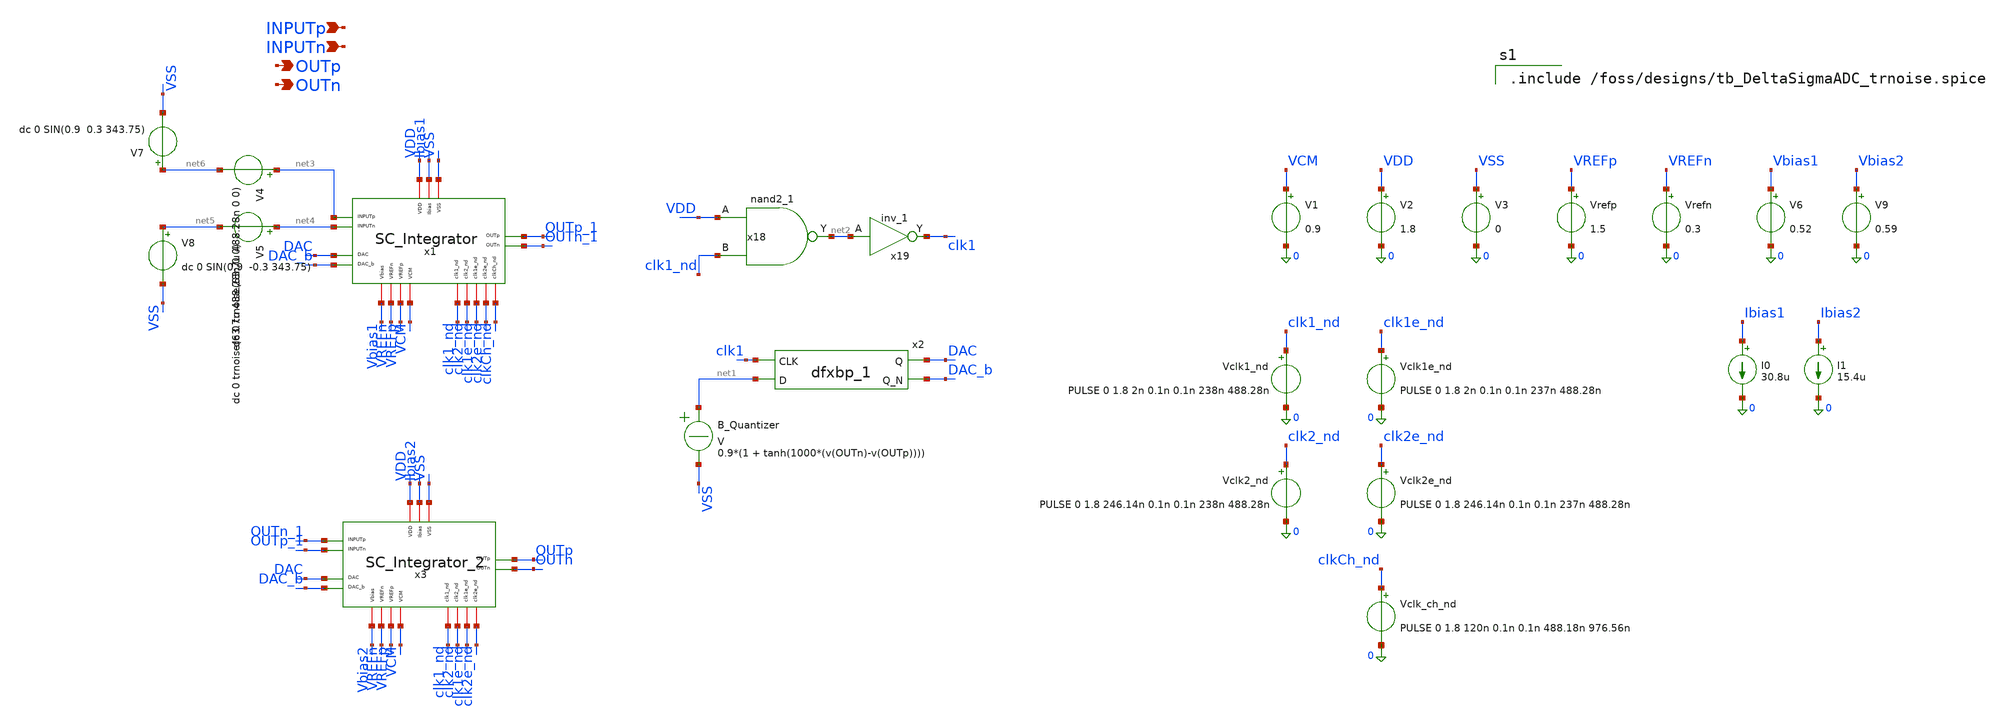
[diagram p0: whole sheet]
** sch_path: xschem/top/DeltaSigmaADC_L2.sch
**.subckt DeltaSigmaADC_L2 OUTp OUTn INPUTp INPUTn
*.opin OUTp
*.opin OUTn
*.ipin INPUTp
*.ipin INPUTn
x1 VDD clk1_nd OUTp_1 net3 VSS clk2_nd net4 OUTn_1 Ibias1 DAC clk1e_nd VCM DAC_b clk2e_nd VREFp
+ VREFn Vbias1 clkCh_nd SC_Integrator
V1 VCM 0 0.9
V2 VDD 0 1.8
I0 Ibias1 0 30.8u
V3 VSS 0 0
Vrefp VREFp 0 1.5
Vrefn VREFn 0 0.3
V6 Vbias1 0 0.52
Vclk1_nd clk1_nd 0 PULSE 0 1.8 2n 0.1n 0.1n 238n 488.28n
Vclk1e_nd clk1e_nd 0 PULSE 0 1.8 2n 0.1n 0.1n 237n 488.28n
Vclk2_nd clk2_nd 0 PULSE 0 1.8 246.14n 0.1n 0.1n 238n 488.28n
Vclk2e_nd clk2e_nd 0 PULSE 0 1.8 246.14n 0.1n 0.1n 237n 488.28n
B_Quantizer net1 VSS V = 0.9*(1 + tanh(1000*(v(OUTn)-v(OUTp))))
x2 clk1 net1 VSS VSS VDD VDD DAC DAC_b sky130_fd_sc_hd__dfxbp_1
x18 VDD clk1_nd VSS VSS VDD VDD net2 sky130_fd_sc_hd__nand2_1
x19 net2 VSS VSS VDD VDD clk1 sky130_fd_sc_hd__inv_1
x3 VDD clk1_nd OUTp OUTn_1 VSS clk2_nd OUTp_1 OUTn Ibias2 DAC clk1e_nd VCM DAC_b clk2e_nd VREFp
+ VREFn Vbias2 SC_Integrator_2
I1 Ibias2 0 15.4u
Vclk_ch_nd clkCh_nd 0 PULSE 0 1.8 120n 0.1n 0.1n 488.18n 976.56n
V4 net3 net6 dc 0 trnoise(63.7u 488.28n 0 0)
V5 net4 net5 dc 0 trnoise(63.7u 488.28n 0 0)
V7 net6 VSS dc 0 SIN(0.9 0.3 343.75)
V8 net5 VSS dc 0 SIN(0.9 -0.3 343.75)
V9 Vbias2 0 0.59
**** begin user architecture code

.include /foss/designs/tb_DeltaSigmaADC_trnoise.spice

**** end user architecture code
**.ends

* expanding   symbol:  Analog/SC_Integrator.sym # of pins=18
** sym_path: xschem/lib/Analog/SC_Integrator.sym
** sch_path: xschem/lib/Analog/SC_Integrator.sch
.subckt SC_Integrator VDD clk1_nd OUTp INPUTp VSS clk2_nd INPUTn OUTn Ibias DAC clk1e_nd VCM DAC_b
+ clk2e_nd VREFp VREFn Vbias clkCh_nd
*.iopin clk2e_nd
*.iopin clk1e_nd
*.iopin clk2_nd
*.iopin clk1_nd
*.iopin VDD
*.iopin VSS
*.iopin VCM
*.iopin Ibias
*.ipin INPUTp
*.ipin INPUTn
*.iopin VREFp
*.iopin VREFn
*.iopin Vbias
*.ipin DAC
*.ipin DAC_b
*.opin OUTp
*.opin OUTn
*.iopin clkCh_nd
x1 VDD Ibias net13 OTA_OUTp OTA_OUTn net4 VSS CMFB FullyDiffOTA
x14 DAC_b clk2_nd VSS VSS VDD VDD clkDn_b sky130_fd_sc_hd__nand2_1
x15 clkDn_b VSS VSS VDD VDD clkDn sky130_fd_sc_hd__inv_1
x16 DAC clk2_nd VSS VSS VDD VDD clkDp_b sky130_fd_sc_hd__nand2_1
x17 clkDp_b VSS VSS VDD VDD clkDp sky130_fd_sc_hd__inv_1
x18 VDD clk1_nd VSS VSS VDD VDD clk1_b sky130_fd_sc_hd__nand2_1
x19 clk1_b VSS VSS VDD VDD clk1 sky130_fd_sc_hd__inv_1
x20 VDD clk2_nd VSS VSS VDD VDD clk2_b sky130_fd_sc_hd__nand2_1
x21 clk2_b VSS VSS VDD VDD clk2 sky130_fd_sc_hd__inv_1
x10 VDD clk1e_nd VSS VSS VDD VDD clk1e_b sky130_fd_sc_hd__nand2_1
x25 clk1e_b VSS VSS VDD VDD clk1e sky130_fd_sc_hd__inv_1
x26 VDD clk2e_nd VSS VSS VDD VDD clk2e_b sky130_fd_sc_hd__nand2_1
x27 clk2e_b VSS VSS VDD VDD clk2e sky130_fd_sc_hd__inv_1
XC16 net1 net2 sky130_fd_pr__cap_mim_m3_2 W=15 L=10 MF=6 m=6
XC17 net1 net2 sky130_fd_pr__cap_mim_m3_1 W=19 L=10 MF=6 m=6
XC2 OUTp INn sky130_fd_pr__cap_mim_m3_2 W=15 L=10 MF=20 m=20
XC3 OUTp INn sky130_fd_pr__cap_mim_m3_1 W=19 L=10 MF=20 m=20
XM2 VREFp clkDp_b net7 VDD sky130_fd_pr__pfet_01v8 L=0.15 W=2 nf=1 ad='int((1 + 1)/2) * 2 / 1 * 0.29'
+ as='int((1 + 2)/2) * 2 / 1 * 0.29' pd='2*int((1 + 1)/2) * (2 / 1 + 0.29)' ps='2*int((1 + 2)/2) * (2 / 1 + 0.29)'
+ nrd='0.29 / 2 ' nrs='0.29 / 2 ' sa=0 sb=0 sd=0 mult=1 m=1
XM1 VREFp clkDn_b net3 VDD sky130_fd_pr__pfet_01v8 L=0.15 W=2 nf=1 ad='int((1 + 1)/2) * 2 / 1 * 0.29'
+ as='int((1 + 2)/2) * 2 / 1 * 0.29' pd='2*int((1 + 1)/2) * (2 / 1 + 0.29)' ps='2*int((1 + 2)/2) * (2 / 1 + 0.29)'
+ nrd='0.29 / 2 ' nrs='0.29 / 2 ' sa=0 sb=0 sd=0 mult=1 m=1
XM3 VREFn clkDn net7 VSS sky130_fd_pr__nfet_01v8 L=0.15 W=1 nf=1 ad='int((1 + 1)/2) * 1 / 1 * 0.29' as='int((1 + 2)/2) * 1 / 1 * 0.29'
+ pd='2*int((1 + 1)/2) * (1 / 1 + 0.29)' ps='2*int((1 + 2)/2) * (1 / 1 + 0.29)' nrd='0.29 / 1 ' nrs='0.29 / 1 '
+ sa=0 sb=0 sd=0 mult=1 m=1
XM4 VREFn clkDp net3 VSS sky130_fd_pr__nfet_01v8 L=0.15 W=1 nf=1 ad='int((1 + 1)/2) * 1 / 1 * 0.29' as='int((1 + 2)/2) * 1 / 1 * 0.29'
+ pd='2*int((1 + 1)/2) * (1 / 1 + 0.29)' ps='2*int((1 + 2)/2) * (1 / 1 + 0.29)' nrd='0.29 / 1 ' nrs='0.29 / 1 '
+ sa=0 sb=0 sd=0 mult=1 m=1
x4 clk1_b clk1 VDD VSS INPUTn net2 Bootstrap_Switch Wn=1.0 Wp=1.0 LL=0.15
x3 clk1_b clk1 VDD VSS INPUTp net6 Bootstrap_Switch Wn=1.0 Wp=1.0 LL=0.15
x6 clk1e_b clk1e VDD VSS net1 VCM TG_switch Wn=3.0 Wp=10.0 LL=0.35
x9 clk1e_b clk1e VDD VSS net5 VCM TG_switch Wn=3.0 Wp=10.0 LL=0.35
x2 clk2_b clk2 VDD VSS VCM net2 TG_switch Wn=3.0 Wp=10.0 LL=0.35
x5 clk1_b clk1 VDD VSS VCM net3 TG_switch Wn=3.0 Wp=10.0 LL=0.35
x8 clk2_b clk2 VDD VSS VCM net6 TG_switch Wn=3.0 Wp=10.0 LL=0.35
x11 clk1_b clk1 VDD VSS VCM net7 TG_switch Wn=3.0 Wp=10.0 LL=0.35
x7 clk2e_b clk2e VDD VSS net1 INn TG_switch Wn=4.0 Wp=14.0 LL=0.35
x13 clk2e_b clk2e VDD VSS net5 INp TG_switch Wn=4.0 Wp=14.0 LL=0.35
XC14 CMFB OTA_OUTp sky130_fd_pr__cap_mim_m3_2 W=15 L=10 MF=1 m=1
XC15 CMFB OTA_OUTp sky130_fd_pr__cap_mim_m3_1 W=10 L=10 MF=1 m=1
XC18 CMFB OTA_OUTn sky130_fd_pr__cap_mim_m3_2 W=15 L=10 MF=1 m=1
XC19 CMFB OTA_OUTn sky130_fd_pr__cap_mim_m3_1 W=10 L=10 MF=1 m=1
x23 clk1_b clk1 VDD VSS OTA_OUTn net8 TG_switch Wn=3.0 Wp=10.0 LL=0.35
x12 clk1_b clk1 VDD VSS CMFB net9 TG_switch Wn=3.0 Wp=10.0 LL=0.35
x22 clk2_b clk2 VDD VSS VCM net8 TG_switch Wn=3.0 Wp=10.0 LL=0.35
x24 clk2_b clk2 VDD VSS Vbias net9 TG_switch Wn=3.0 Wp=10.0 LL=0.35
XC20 net9 net8 sky130_fd_pr__cap_mim_m3_2 W=3 L=2 MF=5 m=5
XC21 net9 net8 sky130_fd_pr__cap_mim_m3_1 W=3 L=2 MF=5 m=5
x28 clk1_b clk1 VDD VSS OTA_OUTp net10 TG_switch Wn=3.0 Wp=10.0 LL=0.35
x29 clk1_b clk1 VDD VSS CMFB net11 TG_switch Wn=3.0 Wp=10.0 LL=0.35
x30 clk2_b clk2 VDD VSS VCM net10 TG_switch Wn=3.0 Wp=10.0 LL=0.35
x31 clk2_b clk2 VDD VSS Vbias net11 TG_switch Wn=3.0 Wp=10.0 LL=0.35
XC22 net11 net10 sky130_fd_pr__cap_mim_m3_2 W=3 L=2 MF=5 m=5
XC23 net11 net10 sky130_fd_pr__cap_mim_m3_1 W=3 L=2 MF=5 m=5
x32 clkCh VDD clkCh_b VSS net12 INn net4 INp chopper
x33 clkCh VDD clkCh_b VSS OUTp OTA_OUTp OUTn OTA_OUTn chopper
x34 VDD clkCh_nd VSS VSS VDD VDD clkCh_b sky130_fd_sc_hd__nand2_1
x35 clkCh_b VSS VSS VDD VDD clkCh sky130_fd_sc_hd__inv_1
Vflicker net13 net12 dc 0 trnoise(0 1u 0.85 66.4u)
XC1 net1 net3 sky130_fd_pr__cap_mim_m3_2 W=15 L=10 MF=6 m=6
XC4 net1 net3 sky130_fd_pr__cap_mim_m3_1 W=19 L=10 MF=6 m=6
XC5 net5 net6 sky130_fd_pr__cap_mim_m3_2 W=15 L=10 MF=6 m=6
XC6 net5 net6 sky130_fd_pr__cap_mim_m3_1 W=19 L=10 MF=6 m=6
XC7 net5 net7 sky130_fd_pr__cap_mim_m3_2 W=15 L=10 MF=6 m=6
XC8 net5 net7 sky130_fd_pr__cap_mim_m3_1 W=19 L=10 MF=6 m=6
XC9 OUTn INp sky130_fd_pr__cap_mim_m3_2 W=15 L=10 MF=20 m=20
XC10 OUTn INp sky130_fd_pr__cap_mim_m3_1 W=19 L=10 MF=20 m=20
.ends


* expanding   symbol:  Analog/SC_Integrator_2.sym # of pins=17
** sym_path: xschem/lib/Analog/SC_Integrator_2.sym
** sch_path: xschem/lib/Analog/SC_Integrator_2.sch
.subckt SC_Integrator_2 VDD clk1_nd OUTp INPUTp VSS clk2_nd INPUTn OUTn Ibias DAC clk1e_nd VCM DAC_b
+ clk2e_nd VREFp VREFn Vbias
*.iopin clk2e_nd
*.iopin clk1e_nd
*.iopin clk2_nd
*.iopin clk1_nd
*.iopin VDD
*.iopin VSS
*.iopin VCM
*.iopin Ibias
*.ipin INPUTp
*.ipin INPUTn
*.iopin VREFp
*.iopin VREFn
*.iopin Vbias
*.ipin DAC
*.ipin DAC_b
*.opin OUTp
*.opin OUTn
x14 DAC_b clk2_nd VSS VSS VDD VDD clkDn_b sky130_fd_sc_hd__nand2_1
x15 clkDn_b VSS VSS VDD VDD clkDn sky130_fd_sc_hd__inv_1
x16 DAC clk2_nd VSS VSS VDD VDD clkDp_b sky130_fd_sc_hd__nand2_1
x17 clkDp_b VSS VSS VDD VDD clkDp sky130_fd_sc_hd__inv_1
x18 VDD clk1_nd VSS VSS VDD VDD clk1_b sky130_fd_sc_hd__nand2_1
x19 clk1_b VSS VSS VDD VDD clk1 sky130_fd_sc_hd__inv_1
x20 VDD clk2_nd VSS VSS VDD VDD clk2_b sky130_fd_sc_hd__nand2_1
x21 clk2_b VSS VSS VDD VDD clk2 sky130_fd_sc_hd__inv_1
x10 VDD clk1e_nd VSS VSS VDD VDD clk1e_b sky130_fd_sc_hd__nand2_1
x25 clk1e_b VSS VSS VDD VDD clk1e sky130_fd_sc_hd__inv_1
x26 VDD clk2e_nd VSS VSS VDD VDD clk2e_b sky130_fd_sc_hd__nand2_1
x27 clk2e_b VSS VSS VDD VDD clk2e sky130_fd_sc_hd__inv_1
XM2 VREFp clkDp_b net6 VDD sky130_fd_pr__pfet_01v8 L=0.15 W=2 nf=1 ad='int((1 + 1)/2) * 2 / 1 * 0.29'
+ as='int((1 + 2)/2) * 2 / 1 * 0.29' pd='2*int((1 + 1)/2) * (2 / 1 + 0.29)' ps='2*int((1 + 2)/2) * (2 / 1 + 0.29)'
+ nrd='0.29 / 2 ' nrs='0.29 / 2 ' sa=0 sb=0 sd=0 mult=1 m=1
XM1 VREFp clkDn_b net3 VDD sky130_fd_pr__pfet_01v8 L=0.15 W=2 nf=1 ad='int((1 + 1)/2) * 2 / 1 * 0.29'
+ as='int((1 + 2)/2) * 2 / 1 * 0.29' pd='2*int((1 + 1)/2) * (2 / 1 + 0.29)' ps='2*int((1 + 2)/2) * (2 / 1 + 0.29)'
+ nrd='0.29 / 2 ' nrs='0.29 / 2 ' sa=0 sb=0 sd=0 mult=1 m=1
XM3 VREFn clkDn net6 VSS sky130_fd_pr__nfet_01v8 L=0.15 W=1 nf=1 ad='int((1 + 1)/2) * 1 / 1 * 0.29' as='int((1 + 2)/2) * 1 / 1 * 0.29'
+ pd='2*int((1 + 1)/2) * (1 / 1 + 0.29)' ps='2*int((1 + 2)/2) * (1 / 1 + 0.29)' nrd='0.29 / 1 ' nrs='0.29 / 1 '
+ sa=0 sb=0 sd=0 mult=1 m=1
XM4 VREFn clkDp net3 VSS sky130_fd_pr__nfet_01v8 L=0.15 W=1 nf=1 ad='int((1 + 1)/2) * 1 / 1 * 0.29' as='int((1 + 2)/2) * 1 / 1 * 0.29'
+ pd='2*int((1 + 1)/2) * (1 / 1 + 0.29)' ps='2*int((1 + 2)/2) * (1 / 1 + 0.29)' nrd='0.29 / 1 ' nrs='0.29 / 1 '
+ sa=0 sb=0 sd=0 mult=1 m=1
x4 clk1_b clk1 VDD VSS INPUTn net2 Bootstrap_Switch Wn=1.0 Wp=1.0 LL=0.15
x3 clk1_b clk1 VDD VSS INPUTp net5 Bootstrap_Switch Wn=1.0 Wp=1.0 LL=0.15
x6 clk1e_b clk1e VDD VSS net1 VCM TG_switch Wn=3.0 Wp=10.0 LL=0.35
x9 clk1e_b clk1e VDD VSS net4 VCM TG_switch Wn=3.0 Wp=10.0 LL=0.35
x2 clk2_b clk2 VDD VSS VCM net2 TG_switch Wn=3.0 Wp=10.0 LL=0.35
x5 clk1_b clk1 VDD VSS VCM net3 TG_switch Wn=3.0 Wp=10.0 LL=0.35
x8 clk2_b clk2 VDD VSS VCM net5 TG_switch Wn=3.0 Wp=10.0 LL=0.35
x11 clk1_b clk1 VDD VSS VCM net6 TG_switch Wn=3.0 Wp=10.0 LL=0.35
x7 clk2e_b clk2e VDD VSS net1 INn TG_switch Wn=4.0 Wp=14.0 LL=0.35
x13 clk2e_b clk2e VDD VSS net4 INp TG_switch Wn=4.0 Wp=14.0 LL=0.35
XC14 CMFB OUTp sky130_fd_pr__cap_mim_m3_2 W=15 L=10 MF=1 m=1
XC15 CMFB OUTp sky130_fd_pr__cap_mim_m3_1 W=10 L=10 MF=1 m=1
XC18 CMFB OUTn sky130_fd_pr__cap_mim_m3_2 W=15 L=10 MF=1 m=1
XC19 CMFB OUTn sky130_fd_pr__cap_mim_m3_1 W=10 L=10 MF=1 m=1
x23 clk1_b clk1 VDD VSS OUTn net7 TG_switch Wn=3.0 Wp=10.0 LL=0.35
x12 clk1_b clk1 VDD VSS CMFB net8 TG_switch Wn=3.0 Wp=10.0 LL=0.35
x22 clk2_b clk2 VDD VSS VCM net7 TG_switch Wn=3.0 Wp=10.0 LL=0.35
x24 clk2_b clk2 VDD VSS Vbias net8 TG_switch Wn=3.0 Wp=10.0 LL=0.35
XC20 net8 net7 sky130_fd_pr__cap_mim_m3_2 W=3 L=2 MF=5 m=5
XC21 net8 net7 sky130_fd_pr__cap_mim_m3_1 W=3 L=2 MF=5 m=5
x28 clk1_b clk1 VDD VSS OUTp net9 TG_switch Wn=3.0 Wp=10.0 LL=0.35
x29 clk1_b clk1 VDD VSS CMFB net10 TG_switch Wn=3.0 Wp=10.0 LL=0.35
x30 clk2_b clk2 VDD VSS VCM net9 TG_switch Wn=3.0 Wp=10.0 LL=0.35
x31 clk2_b clk2 VDD VSS Vbias net10 TG_switch Wn=3.0 Wp=10.0 LL=0.35
XC22 net10 net9 sky130_fd_pr__cap_mim_m3_2 W=3 L=2 MF=5 m=5
XC23 net10 net9 sky130_fd_pr__cap_mim_m3_1 W=3 L=2 MF=5 m=5
XC4 net1 net2 sky130_fd_pr__cap_mim_m3_2 W=10 L=5 MF=20 m=20
XC6 net1 net2 sky130_fd_pr__cap_mim_m3_1 W=10 L=5 MF=20 m=20
XC8 net4 net5 sky130_fd_pr__cap_mim_m3_2 W=10 L=5 MF=20 m=20
XC9 net4 net5 sky130_fd_pr__cap_mim_m3_1 W=10 L=5 MF=20 m=20
XC10 net1 net3 sky130_fd_pr__cap_mim_m3_2 W=10 L=5 MF=12 m=12
XC11 net1 net3 sky130_fd_pr__cap_mim_m3_1 W=10 L=5 MF=12 m=12
XC16 net4 net6 sky130_fd_pr__cap_mim_m3_2 W=10 L=5 MF=12 m=12
XC17 net4 net6 sky130_fd_pr__cap_mim_m3_1 W=10 L=5 MF=12 m=12
XC2 OUTp INn sky130_fd_pr__cap_mim_m3_2 W=10 L=5 MF=33 m=33
XC3 OUTp INn sky130_fd_pr__cap_mim_m3_1 W=10 L=5 MF=33 m=33
XC12 OUTn INp sky130_fd_pr__cap_mim_m3_2 W=10 L=5 MF=33 m=33
XC13 OUTn INp sky130_fd_pr__cap_mim_m3_1 W=10 L=5 MF=33 m=33
x1 VDD Ibias INn OUTp OUTn INp VSS CMFB FullyDiffOTA_2
.ends


* expanding   symbol:  Analog/FullyDiffOTA.sym # of pins=8
** sym_path: xschem/lib/Analog/FullyDiffOTA.sym
** sch_path: xschem/lib/Analog/FullyDiffOTA.sch
.subckt FullyDiffOTA VDD Ibias INn OUTp OUTn INp VSS CMFB
*.iopin CMFB
*.ipin INp
*.iopin VDD
*.ipin INn
*.iopin VSS
*.opin OUTp
*.opin OUTn
*.iopin Ibias
XItail net1 Ibias VDD VDD sky130_fd_pr__pfet_01v8 L=0.7 W=2.5 nf=1 ad='int((nf+1)/2) * W/nf * 0.29' as='int((nf+2)/2) * W/nf * 0.29'
+ pd='2*int((nf+1)/2) * (W/nf + 0.29)' ps='2*int((nf+2)/2) * (W/nf + 0.29)' nrd='0.29 / W' nrs='0.29 / W'
+ sa=0 sb=0 sd=0 mult=9 m=9
XM1 OUTp1 INp net1 net1 sky130_fd_pr__pfet_01v8_lvt L=1.0 W=7.3 nf=1 ad='int((1 + 1)/2) * 7.3 / 1 * 0.29'
+ as='int((1 + 2)/2) * 7.3 / 1 * 0.29' pd='2*int((1 + 1)/2) * (7.3 / 1 + 0.29)' ps='2*int((1 + 2)/2) * (7.3 / 1 + 0.29)'
+ nrd='0.29 / 7.3 ' nrs='0.29 / 7.3 ' sa=0 sb=0 sd=0 mult=10 m=10
XM2 OUTn1 INn net1 net1 sky130_fd_pr__pfet_01v8_lvt L=1.0 W=7.3 nf=1 ad='int((1 + 1)/2) * 7.3 / 1 * 0.29'
+ as='int((1 + 2)/2) * 7.3 / 1 * 0.29' pd='2*int((1 + 1)/2) * (7.3 / 1 + 0.29)' ps='2*int((1 + 2)/2) * (7.3 / 1 + 0.29)'
+ nrd='0.29 / 7.3 ' nrs='0.29 / 7.3 ' sa=0 sb=0 sd=0 mult=10 m=10
XM3 OUTp1 VCM1 VSS VSS sky130_fd_pr__nfet_01v8 L=0.45 W=2.5 nf=1 ad='int((1 + 1)/2) * 2.5 / 1 * 0.29'
+ as='int((1 + 2)/2) * 2.5 / 1 * 0.29' pd='2*int((1 + 1)/2) * (2.5 / 1 + 0.29)' ps='2*int((1 + 2)/2) * (2.5 / 1 + 0.29)'
+ nrd='0.29 / 2.5 ' nrs='0.29 / 2.5 ' sa=0 sb=0 sd=0 mult=1 m=1
XM4 OUTn1 VCM1 VSS VSS sky130_fd_pr__nfet_01v8 L=0.45 W=2.5 nf=1 ad='int((1 + 1)/2) * 2.5 / 1 * 0.29'
+ as='int((1 + 2)/2) * 2.5 / 1 * 0.29' pd='2*int((1 + 1)/2) * (2.5 / 1 + 0.29)' ps='2*int((1 + 2)/2) * (2.5 / 1 + 0.29)'
+ nrd='0.29 / 2.5 ' nrs='0.29 / 2.5 ' sa=0 sb=0 sd=0 mult=1 m=1
XM5 OUTp OUTp1 VSS VSS sky130_fd_pr__nfet_01v8 L=0.45 W=5 nf=1 ad='int((1 + 1)/2) * 5 / 1 * 0.29' as='int((1 + 2)/2) * 5 / 1 * 0.29'
+ pd='2*int((1 + 1)/2) * (5 / 1 + 0.29)' ps='2*int((1 + 2)/2) * (5 / 1 + 0.29)' nrd='0.29 / 5 ' nrs='0.29 / 5 '
+ sa=0 sb=0 sd=0 mult=3 m=3
XM6 OUTn OUTn1 VSS VSS sky130_fd_pr__nfet_01v8 L=0.45 W=5 nf=1 ad='int((1 + 1)/2) * 5 / 1 * 0.29' as='int((1 + 2)/2) * 5 / 1 * 0.29'
+ pd='2*int((1 + 1)/2) * (5 / 1 + 0.29)' ps='2*int((1 + 2)/2) * (5 / 1 + 0.29)' nrd='0.29 / 5 ' nrs='0.29 / 5 '
+ sa=0 sb=0 sd=0 mult=3 m=3
XM7 OUTp CMFB VDD VDD sky130_fd_pr__pfet_01v8 L=0.45 W=2.5 nf=1 ad='int((1 + 1)/2) * 2.5 / 1 * 0.29'
+ as='int((1 + 2)/2) * 2.5 / 1 * 0.29' pd='2*int((1 + 1)/2) * (2.5 / 1 + 0.29)' ps='2*int((1 + 2)/2) * (2.5 / 1 + 0.29)'
+ nrd='0.29 / 2.5 ' nrs='0.29 / 2.5 ' sa=0 sb=0 sd=0 mult=9 m=9
XM8 OUTn CMFB VDD VDD sky130_fd_pr__pfet_01v8 L=0.45 W=2.5 nf=1 ad='int((1 + 1)/2) * 2.5 / 1 * 0.29'
+ as='int((1 + 2)/2) * 2.5 / 1 * 0.29' pd='2*int((1 + 1)/2) * (2.5 / 1 + 0.29)' ps='2*int((1 + 2)/2) * (2.5 / 1 + 0.29)'
+ nrd='0.29 / 2.5 ' nrs='0.29 / 2.5 ' sa=0 sb=0 sd=0 mult=9 m=9
XM9 Ibias Ibias VDD VDD sky130_fd_pr__pfet_01v8 L=0.7 W=2.5 nf=1 ad='int((nf+1)/2) * W/nf * 0.29' as='int((nf+2)/2) * W/nf * 0.29'
+ pd='2*int((nf+1)/2) * (W/nf + 0.29)' ps='2*int((nf+2)/2) * (W/nf + 0.29)' nrd='0.29 / W' nrs='0.29 / W'
+ sa=0 sb=0 sd=0 mult=9 m=9
XR9 OUTp1 VCM1 VSS sky130_fd_pr__res_xhigh_po_0p35 L=53 mult=1 m=1
XR5 VCM1 OUTn1 VSS sky130_fd_pr__res_xhigh_po_0p35 L=53 mult=1 m=1
XC5 VCM1 OUTp1 sky130_fd_pr__cap_mim_m3_1 W=2 L=3 MF=1 m=1
XC6 OUTp1 VCM1 sky130_fd_pr__cap_mim_m3_2 W=2 L=3 MF=1 m=1
XC3 OUTn1 VCM1 sky130_fd_pr__cap_mim_m3_1 W=2 L=3 MF=1 m=1
XC4 VCM1 OUTn1 sky130_fd_pr__cap_mim_m3_2 W=2 L=3 MF=1 m=1
XR1 net2 OUTp1 VSS sky130_fd_pr__res_high_po W=1 L=2 mult=1 m=1
XR2 OUTn1 net3 VSS sky130_fd_pr__res_high_po W=1 L=2 mult=1 m=1
XC7 net3 OUTn sky130_fd_pr__cap_mim_m3_1 W=12 L=12 MF=2 m=2
XC8 net3 OUTn sky130_fd_pr__cap_mim_m3_2 W=12 L=12 MF=2 m=2
XC1 OUTp net2 sky130_fd_pr__cap_mim_m3_1 W=12 L=12 MF=2 m=2
XC2 OUTp net2 sky130_fd_pr__cap_mim_m3_2 W=12 L=12 MF=2 m=2
.ends


* expanding   symbol:  Analog/Bootstrap_Switch.sym # of pins=6
** sym_path: xschem/lib/Analog/Bootstrap_Switch.sym
** sch_path: xschem/lib/Analog/Bootstrap_Switch.sch
.subckt Bootstrap_Switch clk_bar clk VDD VSS n1 n2  Wn=1.0 Wp=1.0 LL=0.15
*.iopin n2
*.iopin n1
*.iopin VDD
*.iopin VSS
*.ipin clk_bar
*.ipin clk
XM1 n1 G n2 VSS sky130_fd_pr__nfet_01v8 L=LL W=WN nf=1 ad='int((1 + 1)/2) * WN / 1 * 0.29' as='int((1 + 2)/2) * WN / 1 * 0.29'
+ pd='2*int((1 + 1)/2) * (WN / 1 + 0.29)' ps='2*int((1 + 2)/2) * (WN / 1 + 0.29)' nrd='0.29 / WN ' nrs='0.29 / WN '
+ sa=0 sb=0 sd=0 mult=1 m=1
XM2 CBB G n1 VSS sky130_fd_pr__nfet_01v8 L=LL W=WN nf=1 ad='int((1 + 1)/2) * WN / 1 * 0.29' as='int((1 + 2)/2) * WN / 1 * 0.29'
+ pd='2*int((1 + 1)/2) * (WN / 1 + 0.29)' ps='2*int((1 + 2)/2) * (WN / 1 + 0.29)' nrd='0.29 / WN ' nrs='0.29 / WN '
+ sa=0 sb=0 sd=0 mult=1 m=1
XC1 CBT CBB sky130_fd_pr__cap_mim_m3_1 W=3 L=3 MF=5 m=5
XC2 CBT CBB sky130_fd_pr__cap_mim_m3_2 W=3 L=3 MF=5 m=5
XM3 CBB clk_bar VSS VSS sky130_fd_pr__nfet_01v8 L=LL W=WN nf=1 ad='int((1 + 1)/2) * WN / 1 * 0.29' as='int((1 + 2)/2) * WN / 1 * 0.29'
+ pd='2*int((1 + 1)/2) * (WN / 1 + 0.29)' ps='2*int((1 + 2)/2) * (WN / 1 + 0.29)' nrd='0.29 / WN ' nrs='0.29 / WN '
+ sa=0 sb=0 sd=0 mult=1 m=1
XM6 G VDD X VSS sky130_fd_pr__nfet_01v8 L=LL W=WN nf=1 ad='int((1 + 1)/2) * WN / 1 * 0.29' as='int((1 + 2)/2) * WN / 1 * 0.29'
+ pd='2*int((1 + 1)/2) * (WN / 1 + 0.29)' ps='2*int((1 + 2)/2) * (WN / 1 + 0.29)' nrd='0.29 / WN ' nrs='0.29 / WN '
+ sa=0 sb=0 sd=0 mult=1 m=1
XM7 VDD G CBT CBT sky130_fd_pr__pfet_01v8 L=LL W=Wp nf=1 ad='int((1 + 1)/2) * Wp / 1 * 0.29' as='int((1 + 2)/2) * Wp / 1 * 0.29'
+ pd='2*int((1 + 1)/2) * (Wp / 1 + 0.29)' ps='2*int((1 + 2)/2) * (Wp / 1 + 0.29)' nrd='0.29 / Wp ' nrs='0.29 / Wp '
+ sa=0 sb=0 sd=0 mult=1 m=1
XM8 X clk_bar VSS VSS sky130_fd_pr__nfet_01v8 L=LL W=WN nf=1 ad='int((1 + 1)/2) * WN / 1 * 0.29' as='int((1 + 2)/2) * WN / 1 * 0.29'
+ pd='2*int((1 + 1)/2) * (WN / 1 + 0.29)' ps='2*int((1 + 2)/2) * (WN / 1 + 0.29)' nrd='0.29 / WN ' nrs='0.29 / WN '
+ sa=0 sb=0 sd=0 mult=1 m=1
XM4 CBT clk_bar G CBT sky130_fd_pr__pfet_01v8 L=LL W=Wp nf=1 ad='int((1 + 1)/2) * Wp / 1 * 0.29' as='int((1 + 2)/2) * Wp / 1 * 0.29'
+ pd='2*int((1 + 1)/2) * (Wp / 1 + 0.29)' ps='2*int((1 + 2)/2) * (Wp / 1 + 0.29)' nrd='0.29 / Wp ' nrs='0.29 / Wp '
+ sa=0 sb=0 sd=0 mult=1 m=1
.ends


* expanding   symbol:  Analog/TG_switch.sym # of pins=6
** sym_path: xschem/lib/Analog/TG_switch.sym
** sch_path: xschem/lib/Analog/TG_switch.sch
.subckt TG_switch clk_bar clk VDD VSS n1 n2  Wn=3.0 Wp=10.0 LL=0.35
*.iopin n2
*.iopin n1
*.iopin VDD
*.iopin VSS
*.ipin clk_bar
*.ipin clk
XM3 n1 clk n2 VSS sky130_fd_pr__nfet_01v8_lvt L=LL W=Wn nf=1 ad='int((1 + 1)/2) * Wn / 1 * 0.29' as='int((1 + 2)/2) * Wn / 1 * 0.29'
+ pd='2*int((1 + 1)/2) * (Wn / 1 + 0.29)' ps='2*int((1 + 2)/2) * (Wn / 1 + 0.29)' nrd='0.29 / Wn ' nrs='0.29 / Wn '
+ sa=0 sb=0 sd=0 mult=1 m=1
XM4 n1 clk_bar n2 VDD sky130_fd_pr__pfet_01v8_lvt L=LL W=Wp nf=1 ad='int((1 + 1)/2) * Wp / 1 * 0.29'
+ as='int((1 + 2)/2) * Wp / 1 * 0.29' pd='2*int((1 + 1)/2) * (Wp / 1 + 0.29)' ps='2*int((1 + 2)/2) * (Wp / 1 + 0.29)'
+ nrd='0.29 / Wp ' nrs='0.29 / Wp ' sa=0 sb=0 sd=0 mult=1 m=1
.ends


* expanding   symbol:  Analog/chopper.sym # of pins=8
** sym_path: xschem/lib/Analog/chopper.sym
** sch_path: xschem/lib/Analog/chopper.sch
.subckt chopper clk VDD clk_b VSS OUT1 IN1 OUT2 IN2
*.iopin IN1
*.iopin IN2
*.iopin OUT1
*.iopin OUT2
*.iopin clk
*.iopin clk_b
*.iopin VDD
*.iopin VSS
x1 clk_b clk VDD VSS IN1 OUT1 TG_switch Wn=4.0 Wp=14.0 LL=0.35
x2 clk clk_b VDD VSS IN1 OUT2 TG_switch Wn=4.0 Wp=14.0 LL=0.35
x3 clk clk_b VDD VSS IN2 OUT1 TG_switch Wn=4.0 Wp=14.0 LL=0.35
x4 clk_b clk VDD VSS IN2 OUT2 TG_switch Wn=4.0 Wp=14.0 LL=0.35
.ends


* expanding   symbol:  Analog/FullyDiffOTA_2.sym # of pins=8
** sym_path: xschem/lib/Analog/FullyDiffOTA_2.sym
** sch_path: xschem/lib/Analog/FullyDiffOTA_2.sch
.subckt FullyDiffOTA_2 VDD Ibias INn OUTp OUTn INp VSS CMFB
*.iopin CMFB
*.ipin INp
*.iopin VDD
*.ipin INn
*.iopin VSS
*.opin OUTp
*.opin OUTn
*.iopin Ibias
XItail net1 Ibias VDD VDD sky130_fd_pr__pfet_01v8 L=0.7 W=2.5 nf=1 ad='int((nf+1)/2) * W/nf * 0.29' as='int((nf+2)/2) * W/nf * 0.29'
+ pd='2*int((nf+1)/2) * (W/nf + 0.29)' ps='2*int((nf+2)/2) * (W/nf + 0.29)' nrd='0.29 / W' nrs='0.29 / W'
+ sa=0 sb=0 sd=0 mult=9 m=9
XM1 OUTp1 INp net1 net1 sky130_fd_pr__pfet_01v8_lvt L=1.0 W=7.3 nf=1 ad='int((1 + 1)/2) * 7.3 / 1 * 0.29'
+ as='int((1 + 2)/2) * 7.3 / 1 * 0.29' pd='2*int((1 + 1)/2) * (7.3 / 1 + 0.29)' ps='2*int((1 + 2)/2) * (7.3 / 1 + 0.29)'
+ nrd='0.29 / 7.3 ' nrs='0.29 / 7.3 ' sa=0 sb=0 sd=0 mult=10 m=10
XM2 OUTn1 INn net1 net1 sky130_fd_pr__pfet_01v8_lvt L=1.0 W=7.3 nf=1 ad='int((1 + 1)/2) * 7.3 / 1 * 0.29'
+ as='int((1 + 2)/2) * 7.3 / 1 * 0.29' pd='2*int((1 + 1)/2) * (7.3 / 1 + 0.29)' ps='2*int((1 + 2)/2) * (7.3 / 1 + 0.29)'
+ nrd='0.29 / 7.3 ' nrs='0.29 / 7.3 ' sa=0 sb=0 sd=0 mult=10 m=10
XM3 OUTp1 VCM1 VSS VSS sky130_fd_pr__nfet_01v8 L=0.45 W=2.5 nf=1 ad='int((1 + 1)/2) * 2.5 / 1 * 0.29'
+ as='int((1 + 2)/2) * 2.5 / 1 * 0.29' pd='2*int((1 + 1)/2) * (2.5 / 1 + 0.29)' ps='2*int((1 + 2)/2) * (2.5 / 1 + 0.29)'
+ nrd='0.29 / 2.5 ' nrs='0.29 / 2.5 ' sa=0 sb=0 sd=0 mult=1 m=1
XM4 OUTn1 VCM1 VSS VSS sky130_fd_pr__nfet_01v8 L=0.45 W=2.5 nf=1 ad='int((1 + 1)/2) * 2.5 / 1 * 0.29'
+ as='int((1 + 2)/2) * 2.5 / 1 * 0.29' pd='2*int((1 + 1)/2) * (2.5 / 1 + 0.29)' ps='2*int((1 + 2)/2) * (2.5 / 1 + 0.29)'
+ nrd='0.29 / 2.5 ' nrs='0.29 / 2.5 ' sa=0 sb=0 sd=0 mult=1 m=1
XM5 OUTp OUTp1 VSS VSS sky130_fd_pr__nfet_01v8 L=0.45 W=5 nf=1 ad='int((1 + 1)/2) * 5 / 1 * 0.29' as='int((1 + 2)/2) * 5 / 1 * 0.29'
+ pd='2*int((1 + 1)/2) * (5 / 1 + 0.29)' ps='2*int((1 + 2)/2) * (5 / 1 + 0.29)' nrd='0.29 / 5 ' nrs='0.29 / 5 '
+ sa=0 sb=0 sd=0 mult=3 m=3
XM6 OUTn OUTn1 VSS VSS sky130_fd_pr__nfet_01v8 L=0.45 W=5 nf=1 ad='int((1 + 1)/2) * 5 / 1 * 0.29' as='int((1 + 2)/2) * 5 / 1 * 0.29'
+ pd='2*int((1 + 1)/2) * (5 / 1 + 0.29)' ps='2*int((1 + 2)/2) * (5 / 1 + 0.29)' nrd='0.29 / 5 ' nrs='0.29 / 5 '
+ sa=0 sb=0 sd=0 mult=3 m=3
XM7 OUTp CMFB VDD VDD sky130_fd_pr__pfet_01v8 L=0.45 W=2.5 nf=1 ad='int((1 + 1)/2) * 2.5 / 1 * 0.29'
+ as='int((1 + 2)/2) * 2.5 / 1 * 0.29' pd='2*int((1 + 1)/2) * (2.5 / 1 + 0.29)' ps='2*int((1 + 2)/2) * (2.5 / 1 + 0.29)'
+ nrd='0.29 / 2.5 ' nrs='0.29 / 2.5 ' sa=0 sb=0 sd=0 mult=9 m=9
XM8 OUTn CMFB VDD VDD sky130_fd_pr__pfet_01v8 L=0.45 W=2.5 nf=1 ad='int((1 + 1)/2) * 2.5 / 1 * 0.29'
+ as='int((1 + 2)/2) * 2.5 / 1 * 0.29' pd='2*int((1 + 1)/2) * (2.5 / 1 + 0.29)' ps='2*int((1 + 2)/2) * (2.5 / 1 + 0.29)'
+ nrd='0.29 / 2.5 ' nrs='0.29 / 2.5 ' sa=0 sb=0 sd=0 mult=9 m=9
XM9 Ibias Ibias VDD VDD sky130_fd_pr__pfet_01v8 L=0.7 W=2.5 nf=1 ad='int((nf+1)/2) * W/nf * 0.29' as='int((nf+2)/2) * W/nf * 0.29'
+ pd='2*int((nf+1)/2) * (W/nf + 0.29)' ps='2*int((nf+2)/2) * (W/nf + 0.29)' nrd='0.29 / W' nrs='0.29 / W'
+ sa=0 sb=0 sd=0 mult=9 m=9
XR9 OUTp1 VCM1 VSS sky130_fd_pr__res_xhigh_po_0p35 L=53 mult=1 m=1
XR5 VCM1 OUTn1 VSS sky130_fd_pr__res_xhigh_po_0p35 L=53 mult=1 m=1
XC5 VCM1 OUTp1 sky130_fd_pr__cap_mim_m3_1 W=2 L=3 MF=1 m=1
XC6 OUTp1 VCM1 sky130_fd_pr__cap_mim_m3_2 W=2 L=3 MF=1 m=1
XC3 OUTn1 VCM1 sky130_fd_pr__cap_mim_m3_1 W=2 L=3 MF=1 m=1
XC4 VCM1 OUTn1 sky130_fd_pr__cap_mim_m3_2 W=2 L=3 MF=1 m=1
XR1 net2 OUTp1 VSS sky130_fd_pr__res_high_po W=1 L=2 mult=1 m=1
XR2 OUTn1 net3 VSS sky130_fd_pr__res_high_po W=1 L=2 mult=1 m=1
XC1 OUTp net2 sky130_fd_pr__cap_mim_m3_1 W=12 L=12 MF=1 m=1
XC2 OUTp net2 sky130_fd_pr__cap_mim_m3_1 W=12 L=12 MF=1 m=1
XC7 net3 OUTn sky130_fd_pr__cap_mim_m3_1 W=12 L=12 MF=1 m=1
XC8 net3 OUTn sky130_fd_pr__cap_mim_m3_1 W=12 L=12 MF=1 m=1
.ends

.end
